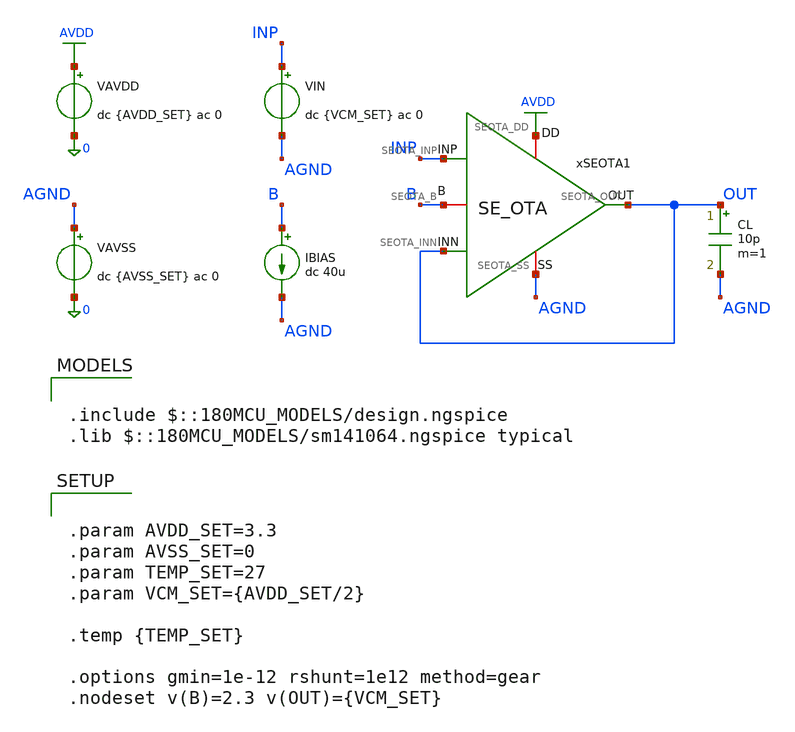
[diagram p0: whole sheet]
** sch_path: Design_Files/IC Design/Testbench/SE_OTA/Close_Loop/SE_OTA_TB_CL_NOM.sch
**.subckt SE_OTA_TB_CL_NOM
CL OUT AGND 10p m=1
xSEOTA1 AVDD AGND INP OUT OUT B SE_OTA
IBIAS B AGND dc 40u
VAVDD AVDD 0 dc {AVDD_SET} ac 0
.save i(vavdd)
VIN INP AGND dc {VCM_SET} ac 0
VAVSS AGND 0 dc {AVSS_SET} ac 0
.save i(vavss)
**** begin user architecture code

.include $::180MCU_MODELS/design.ngspice
.lib $::180MCU_MODELS/sm141064.ngspice typical



.control
destroy all
save all
set wr_vecnames
set wr_singlescale

shell mkdir -p
+ /foss/designs/ECG_Acquisition_IC/Measurement_Results/IC_Simulation/SE_OTA/NOM.Result_txt

shell rm -f
+ /foss/designs/ECG_Acquisition_IC/Measurement_Results/IC_Simulation/SE_OTA/NOM.Result_txt/NOM.cl_dc.txt
shell rm -f
+ /foss/designs/ECG_Acquisition_IC/Measurement_Results/IC_Simulation/SE_OTA/NOM.Result_txt/NOM.cl_tran.txt

let avdd_run = 3.3

* CL DC
dc VIN 0 $&avdd_run 0.001

let cl_vin   = v(inp) - v(agnd)
let cl_vout  = v(out) - v(agnd)
let cl_ibias = 40e-6
let cl_idd   = -vavdd#branch
let cl_iout  = 0

wrdata
+ /foss/designs/ECG_Acquisition_IC/Measurement_Results/IC_Simulation/SE_OTA/NOM.Result_txt/NOM.cl_dc.txt cl_vin cl_vout cl_ibias cl_idd cl_iout

* CL TRAN
alter @VIN[PULSE] = [ 1.0 2.0 1u 1n 1n 10u 20u 0 ]

tran 1n 30u

let tr_vin   = v(inp) - v(agnd)
let tr_vout  = v(out) - v(agnd)
let tr_idd   = -vavdd#branch
let tr_iout  = 10e-12*deriv(tr_vout)

wrdata
+ /foss/designs/ECG_Acquisition_IC/Measurement_Results/IC_Simulation/SE_OTA/NOM.Result_txt/NOM.cl_tran.txt tr_vin tr_vout tr_idd tr_iout

.endc




.param AVDD_SET=3.3
.param AVSS_SET=0
.param TEMP_SET=27
.param VCM_SET={AVDD_SET/2}

.temp {TEMP_SET}

.options gmin=1e-12 rshunt=1e12 method=gear
.nodeset v(B)=2.3 v(OUT)={VCM_SET}


**** end user architecture code
**.ends

* expanding   symbol:  ECG_Acquisition_IC/Design_Files/IC Design/Schematic/SE_OTA/SE_OTA.sym # of
*+ pins=6
** sym_path: Design_Files/IC Design/Schematic/SE_OTA/SE_OTA.sym
** sch_path: Design_Files/IC Design/Schematic/SE_OTA/SE_OTA.sch
.subckt SE_OTA SEOTA_DD SEOTA_SS SEOTA_INP SEOTA_INN SEOTA_OUT SEOTA_B
*.iopin SEOTA_DD
*.iopin SEOTA_SS
*.ipin SEOTA_INP
*.ipin SEOTA_INN
*.opin SEOTA_OUT
*.iopin SEOTA_B
XM3 net4 net4 SEOTA_DD SEOTA_DD pfet_03v3 L=4u W=1u nf=1 ad='int((nf+1)/2) * W/nf * 0.18u' as='int((nf+2)/2) * W/nf * 0.18u'
+ pd='2*int((nf+1)/2) * (W/nf + 0.18u)' ps='2*int((nf+2)/2) * (W/nf + 0.18u)' nrd='0.18u / W' nrs='0.18u / W'
+ sa=0 sb=0 sd=0 m=60
XM7 SEOTA_OUT SEOTA_B SEOTA_SS SEOTA_SS nfet_03v3 L=0.5u W=1u nf=1 ad='int((nf+1)/2) * W/nf * 0.18u'
+ as='int((nf+2)/2) * W/nf * 0.18u' pd='2*int((nf+1)/2) * (W/nf + 0.18u)' ps='2*int((nf+2)/2) * (W/nf + 0.18u)'
+ nrd='0.18u / W' nrs='0.18u / W' sa=0 sb=0 sd=0 m=100
Rz net1 net2 3.8k m=1
XM5 net3 SEOTA_B SEOTA_SS SEOTA_SS nfet_03v3 L=2u W=1u nf=1 ad='int((nf+1)/2) * W/nf * 0.18u' as='int((nf+2)/2) * W/nf * 0.18u'
+ pd='2*int((nf+1)/2) * (W/nf + 0.18u)' ps='2*int((nf+2)/2) * (W/nf + 0.18u)' nrd='0.18u / W' nrs='0.18u / W'
+ sa=0 sb=0 sd=0 m=10
XM6 SEOTA_OUT net1 SEOTA_DD SEOTA_DD pfet_03v3 L=0.5u W=1u nf=1 ad='int((nf+1)/2) * W/nf * 0.18u' as='int((nf+2)/2) * W/nf * 0.18u'
+ pd='2*int((nf+1)/2) * (W/nf + 0.18u)' ps='2*int((nf+2)/2) * (W/nf + 0.18u)' nrd='0.18u / W' nrs='0.18u / W'
+ sa=0 sb=0 sd=0 m=400
XM8 SEOTA_B SEOTA_B SEOTA_SS SEOTA_SS nfet_03v3 L=2u W=1u nf=1 ad='int((nf+1)/2) * W/nf * 0.18u' as='int((nf+2)/2) * W/nf * 0.18u'
+ pd='2*int((nf+1)/2) * (W/nf + 0.18u)' ps='2*int((nf+2)/2) * (W/nf + 0.18u)' nrd='0.18u / W' nrs='0.18u / W'
+ sa=0 sb=0 sd=0 m=20
Cc net2 SEOTA_OUT 2p m=1
XM4 net1 net4 SEOTA_DD SEOTA_DD pfet_03v3 L=4u W=1u nf=1 ad='int((nf+1)/2) * W/nf * 0.18u' as='int((nf+2)/2) * W/nf * 0.18u'
+ pd='2*int((nf+1)/2) * (W/nf + 0.18u)' ps='2*int((nf+2)/2) * (W/nf + 0.18u)' nrd='0.18u / W' nrs='0.18u / W'
+ sa=0 sb=0 sd=0 m=60
XM1 net4 SEOTA_INN net3 SEOTA_SS nfet_03v3 L=4u W=1u nf=1 ad='int((nf+1)/2) * W/nf * 0.18u' as='int((nf+2)/2) * W/nf * 0.18u'
+ pd='2*int((nf+1)/2) * (W/nf + 0.18u)' ps='2*int((nf+2)/2) * (W/nf + 0.18u)' nrd='0.18u / W' nrs='0.18u / W'
+ sa=0 sb=0 sd=0 m=400
XM2 net1 SEOTA_INP net3 SEOTA_SS nfet_03v3 L=4u W=1u nf=1 ad='int((nf+1)/2) * W/nf * 0.18u' as='int((nf+2)/2) * W/nf * 0.18u'
+ pd='2*int((nf+1)/2) * (W/nf + 0.18u)' ps='2*int((nf+2)/2) * (W/nf + 0.18u)' nrd='0.18u / W' nrs='0.18u / W'
+ sa=0 sb=0 sd=0 m=400
.ends

.GLOBAL AVDD
.end
